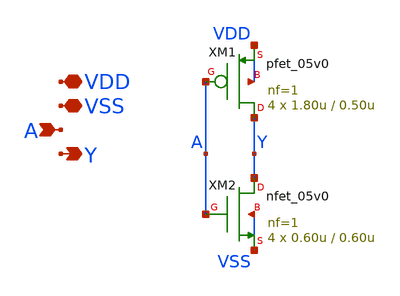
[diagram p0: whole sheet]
** sch_path: xschem/switch-matrix/inv_4.sch
**.subckt inv_4 VDD VSS A Y
*.iopin VDD
*.iopin VSS
*.ipin A
*.opin Y
XM1 Y A VDD VDD pfet_05v0 L=0.50u W=1.80u nf=1 ad='int((nf+1)/2) * W/nf * 0.18u' as='int((nf+2)/2) * W/nf * 0.18u'
+ pd='2*int((nf+1)/2) * (W/nf + 0.18u)' ps='2*int((nf+2)/2) * (W/nf + 0.18u)' nrd='0.18u / W' nrs='0.18u / W'
+ sa=0 sb=0 sd=0 m=4
XM2 Y A VSS VSS nfet_05v0 L=0.60u W=0.60u nf=1 ad='int((nf+1)/2) * W/nf * 0.18u' as='int((nf+2)/2) * W/nf * 0.18u'
+ pd='2*int((nf+1)/2) * (W/nf + 0.18u)' ps='2*int((nf+2)/2) * (W/nf + 0.18u)' nrd='0.18u / W' nrs='0.18u / W'
+ sa=0 sb=0 sd=0 m=4
**.ends
.end
